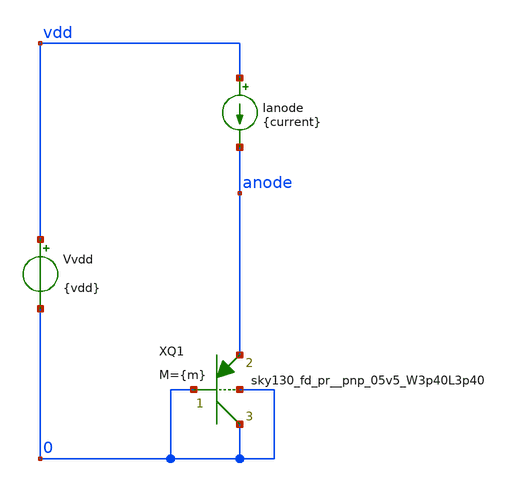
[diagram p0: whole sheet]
** sch_path: xschem/bandgap_core_mod/test/archive/bjt_test.sch
**.subckt bjt_test
XQ1 0 0 anode 0 sky130_fd_pr__pnp_05v5_W3p40L3p40 m={m}
Vvdd vdd 0 {vdd}
Ianode vdd anode {current}
**** begin user architecture code


.temp 27

.lib sky130_fd_pr/models/sky130.lib.spice tt
.include sky130_fd_pr/models/sky130_fd_pr__model__pnp.model.spice

.param vdd=1.8
.param current=1u
.param m=1

.options savecurrents

.dc ianode 0.1e-6 10e-6 0.1e-6


**** end user architecture code
**.ends
.end
